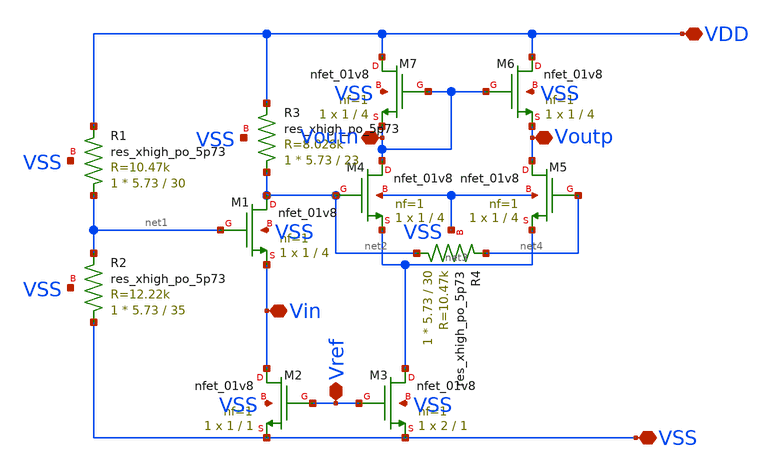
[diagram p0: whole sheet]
** sch_path: hw06/xschem/lna.sch
**.subckt lna VSS VDD Voutp Voutn Vref Vin
*.iopin VSS
*.iopin VDD
*.iopin Voutp
*.iopin Voutn
*.iopin Vref
*.iopin Vin
XR1 net1 VDD VSS sky130_fd_pr__res_xhigh_po_5p73 L=30 mult=1 m=1
XR2 VSS net1 VSS sky130_fd_pr__res_xhigh_po_5p73 L=35 mult=1 m=1
XM1 net2 net1 Vin VSS sky130_fd_pr__nfet_01v8 L=4 W=1 nf=1 ad='int((nf+1)/2) * W/nf * 0.29' as='int((nf+2)/2) * W/nf * 0.29'
+ pd='2*int((nf+1)/2) * (W/nf + 0.29)' ps='2*int((nf+2)/2) * (W/nf + 0.29)' nrd='0.29 / W' nrs='0.29 / W'
+ sa=0 sb=0 sd=0 mult=1 m=1
XM2 Vin Vref VSS VSS sky130_fd_pr__nfet_01v8 L=1 W=1 nf=1 ad='int((nf+1)/2) * W/nf * 0.29' as='int((nf+2)/2) * W/nf * 0.29'
+ pd='2*int((nf+1)/2) * (W/nf + 0.29)' ps='2*int((nf+2)/2) * (W/nf + 0.29)' nrd='0.29 / W' nrs='0.29 / W'
+ sa=0 sb=0 sd=0 mult=1 m=1
XM3 net3 Vref VSS VSS sky130_fd_pr__nfet_01v8 L=1 W=2 nf=1 ad='int((nf+1)/2) * W/nf * 0.29' as='int((nf+2)/2) * W/nf * 0.29'
+ pd='2*int((nf+1)/2) * (W/nf + 0.29)' ps='2*int((nf+2)/2) * (W/nf + 0.29)' nrd='0.29 / W' nrs='0.29 / W'
+ sa=0 sb=0 sd=0 mult=1 m=1
XM4 Voutn net2 net3 VSS sky130_fd_pr__nfet_01v8 L=4 W=1 nf=1 ad='int((nf+1)/2) * W/nf * 0.29' as='int((nf+2)/2) * W/nf * 0.29'
+ pd='2*int((nf+1)/2) * (W/nf + 0.29)' ps='2*int((nf+2)/2) * (W/nf + 0.29)' nrd='0.29 / W' nrs='0.29 / W'
+ sa=0 sb=0 sd=0 mult=1 m=1
XM5 Voutp net4 net3 VSS sky130_fd_pr__nfet_01v8 L=4 W=1 nf=1 ad='int((nf+1)/2) * W/nf * 0.29' as='int((nf+2)/2) * W/nf * 0.29'
+ pd='2*int((nf+1)/2) * (W/nf + 0.29)' ps='2*int((nf+2)/2) * (W/nf + 0.29)' nrd='0.29 / W' nrs='0.29 / W'
+ sa=0 sb=0 sd=0 mult=1 m=1
XM6 VDD Voutn Voutp VSS sky130_fd_pr__nfet_01v8 L=4 W=1 nf=1 ad='int((nf+1)/2) * W/nf * 0.29' as='int((nf+2)/2) * W/nf * 0.29'
+ pd='2*int((nf+1)/2) * (W/nf + 0.29)' ps='2*int((nf+2)/2) * (W/nf + 0.29)' nrd='0.29 / W' nrs='0.29 / W'
+ sa=0 sb=0 sd=0 mult=1 m=1
XM7 VDD Voutn Voutn VSS sky130_fd_pr__nfet_01v8 L=4 W=1 nf=1 ad='int((nf+1)/2) * W/nf * 0.29' as='int((nf+2)/2) * W/nf * 0.29'
+ pd='2*int((nf+1)/2) * (W/nf + 0.29)' ps='2*int((nf+2)/2) * (W/nf + 0.29)' nrd='0.29 / W' nrs='0.29 / W'
+ sa=0 sb=0 sd=0 mult=1 m=1
XR3 net2 VDD VSS sky130_fd_pr__res_xhigh_po_5p73 L=23 mult=1 m=1
XR4 net2 net4 VSS sky130_fd_pr__res_xhigh_po_5p73 L=30 mult=1 m=1
**.ends
.end
